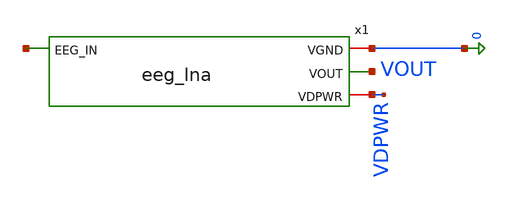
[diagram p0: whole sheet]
** sch_path: xschem/eeg_lna_tb.sch
**.subckt eeg_lna_tb
x1 net1 0 VOUT VDPWR eeg_lna
**** begin user architecture code


.lib /foss/pdks/sky130A/libs.tech/ngspice/sky130.lib.spice tt

.option rshunt=1e12
.option savecurrents

.include /headless/.xschem/simulations/eeg_lna.spice

* =====================================================
* INPUT SIGNALS
* =====================================================

V1 EEG_IN 0 SIN(0 1m 10) DC 0 AC 1
V2 VDPWR 0 DC 1.8

R1 EEG_IN 0 100k

* =====================================================
* ANALYSIS CONTROL
* =====================================================

.control

destroy all
save all

echo "======================================="
echo "EEG LNA DEBUG REPORT"
echo "======================================="

* =====================================================
* OPERATING POINT
* =====================================================

op

echo "======================================="
echo "OPERATING POINT"
echo "======================================="

print v(vout)
print v(eeg_in)

* IMPORTANT INTERNAL NODES
* Change names if needed to match your schematic
print v(x1.vin_p)
print v(x1.vin_n)

print v(x1.tail)
print v(x1.drain_l)
print v(x1.drain_r)

print i(v2)

* =====================================================
* DEVICE OPERATING INFO
* =====================================================

echo "======================================="
echo "MOSFET OPERATING REGIONS"
echo "======================================="

show m.x1.xm1
show m.x1.xm2
show m.x1.xm3
show m.x1.xm4
show m.x1.xm5
show m.x1.xm6
show m.x1.xm7

* =====================================================
* TRANSIENT
* =====================================================

echo "======================================="
echo "TRANSIENT ANALYSIS"
echo "======================================="

tran 100u 200m

plot v(eeg_in)
plot v(vout)

* DIFFERENTIAL INPUT CHECK
plot v(x1.vin_p)-v(x1.vin_n)

* OUTPUT SWING AROUND BIAS
plot v(vout)-avg(v(vout))

* =====================================================
* AC ANALYSIS
* =====================================================

echo "======================================="
echo "AC ANALYSIS"
echo "======================================="

ac dec 20 0.1 10k

* External transfer
plot db(v(vout)/v(eeg_in))

* Internal OTA gain
plot db(v(vout)/v(x1.vin_p))

* Differential gain
plot db(v(vout)/(v(x1.vin_p)-v(x1.vin_n)))

* =====================================================
* NOISE ANALYSIS
* =====================================================

echo "======================================="
echo "NOISE ANALYSIS"
echo "======================================="

noise v(vout) V1 dec 20 0.1 10k 1

setplot noise1

display

* TOTAL OUTPUT NOISE
plot onoise_spectrum xlog ylog

* INPUT REFERRED NOISE
plot inoise_spectrum xlog ylog

* ALL CONTRIBUTORS
plot all xlog ylog

print all

* =====================================================
* SAVE RAW
* =====================================================

write lna_tb.raw

.endc

.end


**** end user architecture code
**.ends

* expanding   symbol:  eeg_lna.sym # of pins=4
** sym_path: xschem/eeg_lna.sym
** sch_path: xschem/eeg_lna.sch
.subckt eeg_lna EEG_IN VGND VOUT VDPWR
*.iopin VGND
*.ipin EEG_IN
*.iopin VDPWR
*.opin VOUT
XM1 MIRROR_BIAS_N MIRROR_BIAS_N VGND VGND sky130_fd_pr__nfet_01v8 L=1.0 W=4 nf=1 ad='int((1 + 1)/2) * 4 / 1 * 0.29'
+ as='int((1 + 2)/2) * 4 / 1 * 0.29' pd='2*int((1 + 1)/2) * (4 / 1 + 0.29)' ps='2*int((1 + 2)/2) * (4 / 1 + 0.29)'
+ nrd='0.29 / 4 ' nrs='0.29 / 4 ' sa=0 sb=0 sd=0 mult=1 m=1
XM2 VOUT MIRROR_BIAS_N VGND VGND sky130_fd_pr__nfet_01v8 L=1.0 W=4 nf=1 ad='int((1 + 1)/2) * 4 / 1 * 0.29'
+ as='int((1 + 2)/2) * 4 / 1 * 0.29' pd='2*int((1 + 1)/2) * (4 / 1 + 0.29)' ps='2*int((1 + 2)/2) * (4 / 1 + 0.29)'
+ nrd='0.29 / 4 ' nrs='0.29 / 4 ' sa=0 sb=0 sd=0 mult=1 m=1
XM3 MIRROR_BIAS_N VIN_P TAIL_P VDPWR sky130_fd_pr__pfet_01v8 L=1.0 W=8 nf=1 ad='int((1 + 1)/2) * 8 / 1 * 0.29'
+ as='int((1 + 2)/2) * 8 / 1 * 0.29' pd='2*int((1 + 1)/2) * (8 / 1 + 0.29)' ps='2*int((1 + 2)/2) * (8 / 1 + 0.29)'
+ nrd='0.29 / 8 ' nrs='0.29 / 8 ' sa=0 sb=0 sd=0 mult=1 m=1
XM4 VOUT VIN_N TAIL_P VDPWR sky130_fd_pr__pfet_01v8 L=1.0 W=8 nf=1 ad='int((1 + 1)/2) * 8 / 1 * 0.29'
+ as='int((1 + 2)/2) * 8 / 1 * 0.29' pd='2*int((1 + 1)/2) * (8 / 1 + 0.29)' ps='2*int((1 + 2)/2) * (8 / 1 + 0.29)'
+ nrd='0.29 / 8 ' nrs='0.29 / 8 ' sa=0 sb=0 sd=0 mult=1 m=1
XM5 TAIL_P BIAS_P VDPWR VDPWR sky130_fd_pr__pfet_01v8 L=1.0 W=8 nf=1 ad='int((1 + 1)/2) * 8 / 1 * 0.29'
+ as='int((1 + 2)/2) * 8 / 1 * 0.29' pd='2*int((1 + 1)/2) * (8 / 1 + 0.29)' ps='2*int((1 + 2)/2) * (8 / 1 + 0.29)'
+ nrd='0.29 / 8 ' nrs='0.29 / 8 ' sa=0 sb=0 sd=0 mult=1 m=1
XM6 BIAS_P BIAS_P VDPWR VDPWR sky130_fd_pr__pfet_01v8 L=1.0 W=4 nf=1 ad='int((1 + 1)/2) * 4 / 1 * 0.29'
+ as='int((1 + 2)/2) * 4 / 1 * 0.29' pd='2*int((1 + 1)/2) * (4 / 1 + 0.29)' ps='2*int((1 + 2)/2) * (4 / 1 + 0.29)'
+ nrd='0.29 / 4 ' nrs='0.29 / 4 ' sa=0 sb=0 sd=0 mult=1 m=1
XM7 BIAS_P BIAS_P VGND VGND sky130_fd_pr__nfet_01v8 L=1.0 W=2 nf=1 ad='int((1 + 1)/2) * 2 / 1 * 0.29'
+ as='int((1 + 2)/2) * 2 / 1 * 0.29' pd='2*int((1 + 1)/2) * (2 / 1 + 0.29)' ps='2*int((1 + 2)/2) * (2 / 1 + 0.29)'
+ nrd='0.29 / 2 ' nrs='0.29 / 2 ' sa=0 sb=0 sd=0 mult=1 m=1
XCIN VIN_P EEG_IN sky130_fd_pr__cap_mim_m3_1 W=20 L=20 MF=1 m=1
RBIAS VIN_P BIAS_P 1Gig m=1
RF VOUT VIN_N 1Meg m=1
RG VIN_N BIAS_P 100k m=1
.ends

.end
